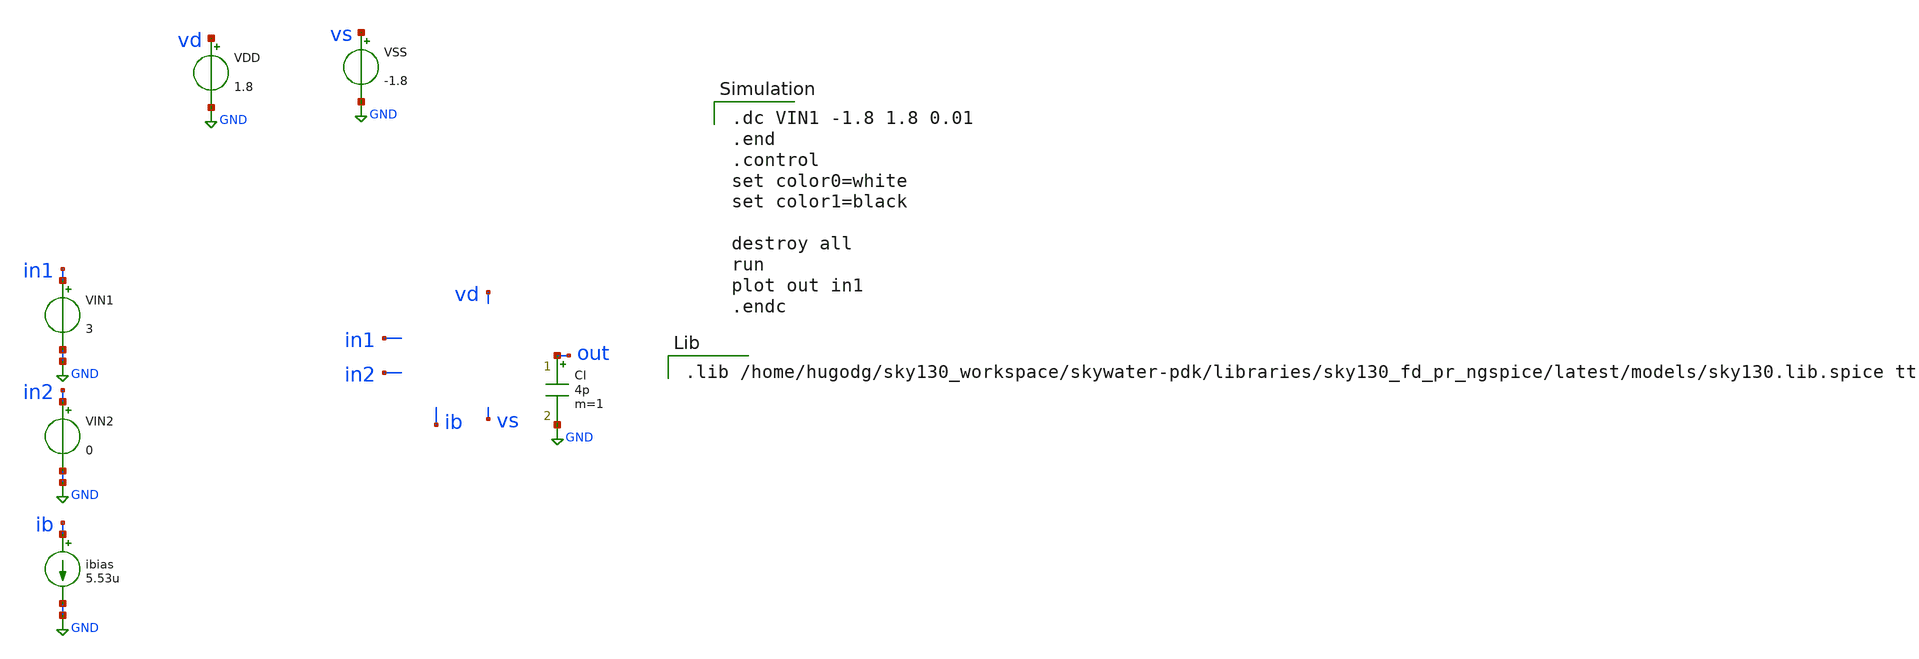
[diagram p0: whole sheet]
** sch_path: mag/sigma-delta_modulator/xschem/sigma_tb-dc.sch
* Copyright 2020 Stefan Frederik Schippers
* Licensed under the Apache License, Version 2.0 (the "License");
* you may not use this file except in compliance with the License.
* You may obtain a copy of the License at
* https://www.apache.org/licenses/LICENSE-2.0
* Unless required by applicable law or agreed to in writing, software
* distributed under the License is distributed on an "AS IS" BASIS,
* WITHOUT WARRANTIES OR CONDITIONS OF ANY KIND, either express or implied.
* See the License for the specific language governing permissions and
* limitations under the License.
**.subckt sigma_tb-dc
VIN2 in2 GND 0
VIN1 in1 GND 3
ibias ib GND 5.53u
VDD vd GND 1.8
VSS vs GND -1.8
Cl out GND 4p m=1
**** begin user architecture code

.dc VIN1 -1.8 1.8 0.01
.end
.control
set color0=white
set color1=black

destroy all
run
plot out in1
.endc


.lib /home/hugodg/sky130_workspace/skywater-pdk/libraries/sky130_fd_pr_ngspice/latest/models/sky130.lib.spice tt

**** end user architecture code
**.ends
.GLOBAL GND
.end
